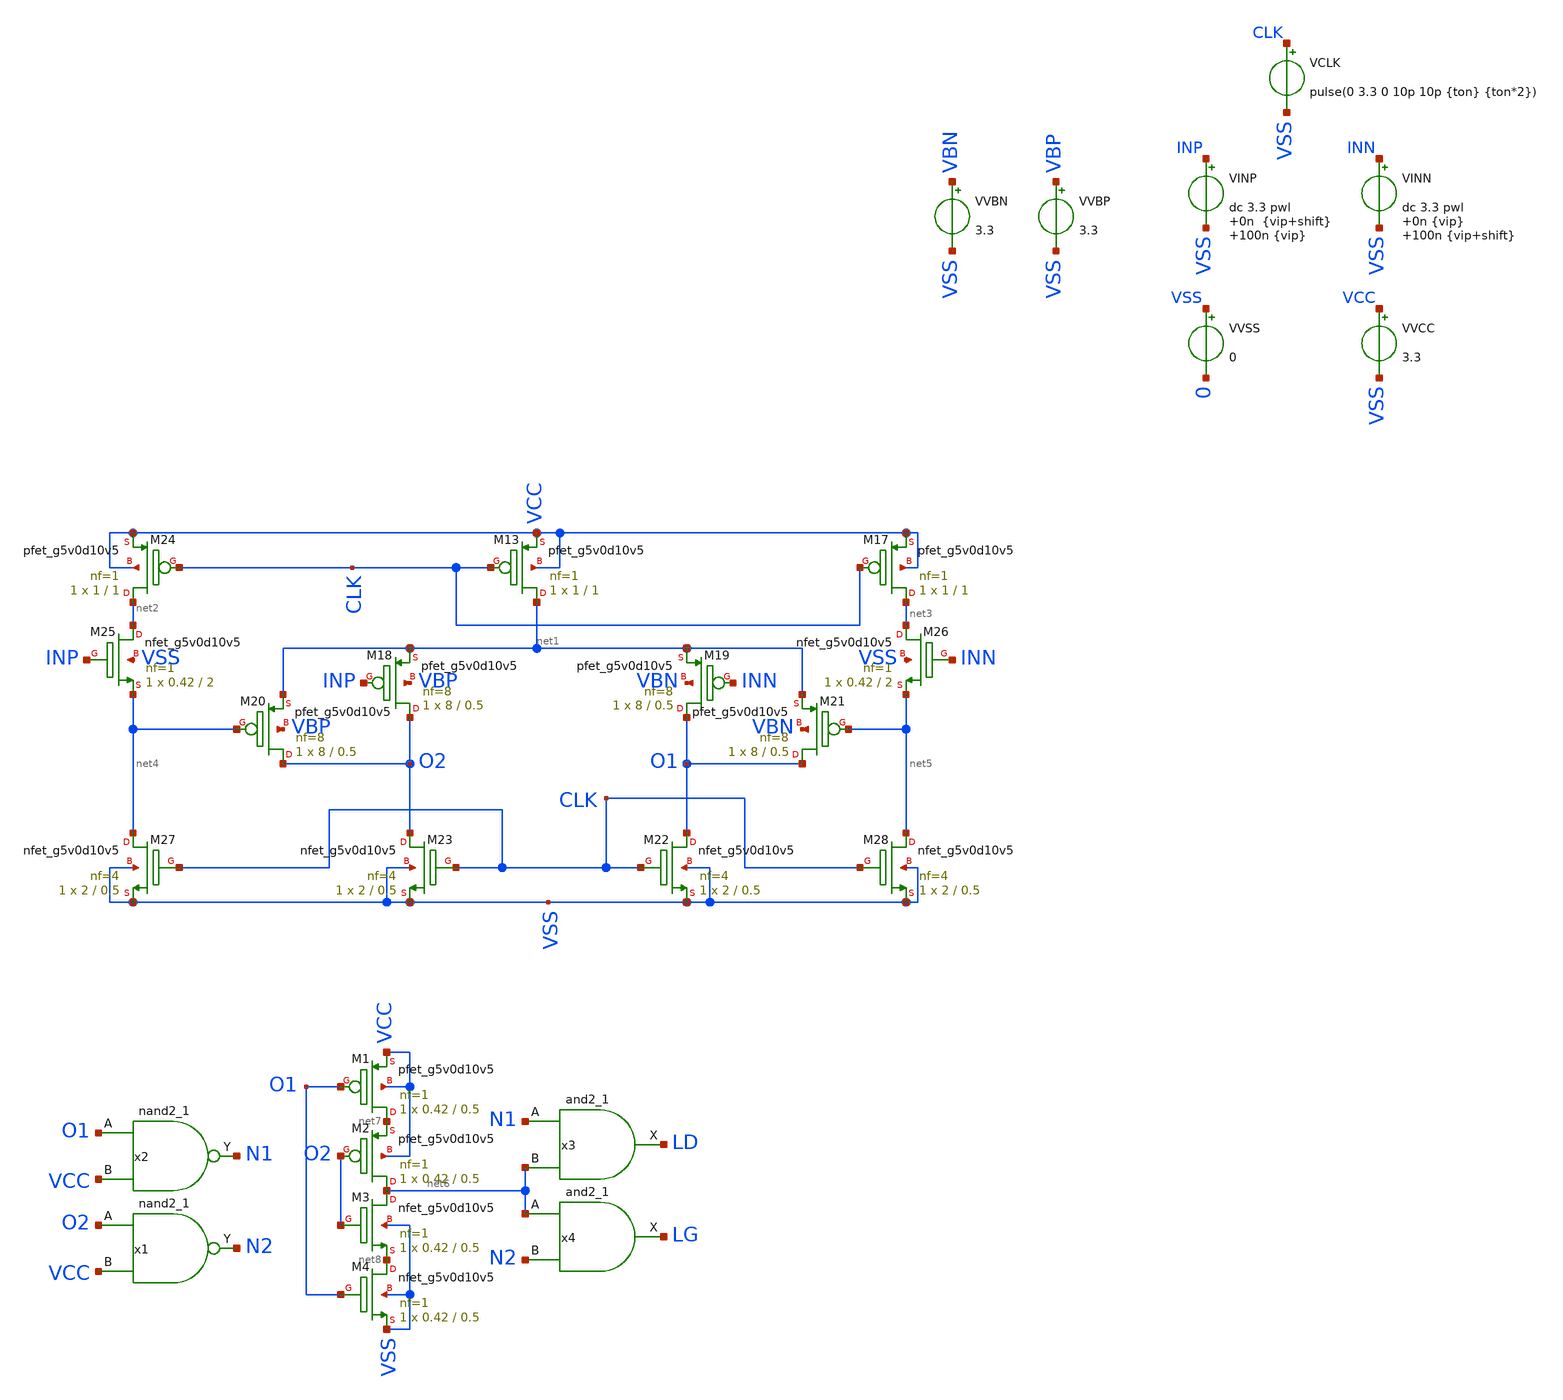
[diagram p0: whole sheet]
** sch_path: Comparator/schematic/new_comparator/c.sch
.lib $::SKYWATER_MODELS/sky130.lib.spice.tt.red tt_mm
.include $::SKYWATER_STDCELLS/sky130_fd_sc_hd.spice

**.subckt c
VINP INP VSS dc 3.3 pwl 0n {vip+shift} 100n {vip}
VINN INN VSS dc 3.3 pwl 0n {vip} 100n {vip+shift}
VVSS VSS 0 0
VVCC VCC VSS 3.3
VCLK CLK VSS pulse(0 3.3 0 10p 10p {ton} {ton*2})
XM13 net1 CLK VCC VCC sky130_fd_pr__pfet_g5v0d10v5 L=1 W=1 nf=1 ad='int((nf+1)/2) * W/nf * 0.29' as='int((nf+2)/2) * W/nf * 0.29'
+ pd='2*int((nf+1)/2) * (W/nf + 0.29)' ps='2*int((nf+2)/2) * (W/nf + 0.29)' nrd='0.29 / W' nrs='0.29 / W'
+ sa=0 sb=0 sd=0 mult=1 m=1
XM17 net3 CLK VCC VCC sky130_fd_pr__pfet_g5v0d10v5 L=1 W=1 nf=1 ad='int((nf+1)/2) * W/nf * 0.29' as='int((nf+2)/2) * W/nf * 0.29'
+ pd='2*int((nf+1)/2) * (W/nf + 0.29)' ps='2*int((nf+2)/2) * (W/nf + 0.29)' nrd='0.29 / W' nrs='0.29 / W'
+ sa=0 sb=0 sd=0 mult=1 m=1
XM18 O2 INP net1 VBP sky130_fd_pr__pfet_g5v0d10v5 L=0.5 W=8 nf=8 ad='int((nf+1)/2) * W/nf * 0.29' as='int((nf+2)/2) * W/nf * 0.29'
+ pd='2*int((nf+1)/2) * (W/nf + 0.29)' ps='2*int((nf+2)/2) * (W/nf + 0.29)' nrd='0.29 / W' nrs='0.29 / W'
+ sa=0 sb=0 sd=0 mult=1 m=1
XM19 O1 INN net1 VBN sky130_fd_pr__pfet_g5v0d10v5 L=0.5 W=8 nf=8 ad='int((nf+1)/2) * W/nf * 0.29' as='int((nf+2)/2) * W/nf * 0.29'
+ pd='2*int((nf+1)/2) * (W/nf + 0.29)' ps='2*int((nf+2)/2) * (W/nf + 0.29)' nrd='0.29 / W' nrs='0.29 / W'
+ sa=0 sb=0 sd=0 mult=1 m=1
XM20 O2 net4 net1 VBP sky130_fd_pr__pfet_g5v0d10v5 L=0.5 W=8 nf=8 ad='int((nf+1)/2) * W/nf * 0.29' as='int((nf+2)/2) * W/nf * 0.29'
+ pd='2*int((nf+1)/2) * (W/nf + 0.29)' ps='2*int((nf+2)/2) * (W/nf + 0.29)' nrd='0.29 / W' nrs='0.29 / W'
+ sa=0 sb=0 sd=0 mult=1 m=1
XM21 O1 net5 net1 VBN sky130_fd_pr__pfet_g5v0d10v5 L=0.5 W=8 nf=8 ad='int((nf+1)/2) * W/nf * 0.29' as='int((nf+2)/2) * W/nf * 0.29'
+ pd='2*int((nf+1)/2) * (W/nf + 0.29)' ps='2*int((nf+2)/2) * (W/nf + 0.29)' nrd='0.29 / W' nrs='0.29 / W'
+ sa=0 sb=0 sd=0 mult=1 m=1
XM22 O1 CLK VSS VSS sky130_fd_pr__nfet_g5v0d10v5 L=0.5 W=2 nf=4 ad='int((nf+1)/2) * W/nf * 0.29' as='int((nf+2)/2) * W/nf * 0.29'
+ pd='2*int((nf+1)/2) * (W/nf + 0.29)' ps='2*int((nf+2)/2) * (W/nf + 0.29)' nrd='0.29 / W' nrs='0.29 / W'
+ sa=0 sb=0 sd=0 mult=1 m=1
XM23 O2 CLK VSS VSS sky130_fd_pr__nfet_g5v0d10v5 L=0.5 W=2 nf=4 ad='int((nf+1)/2) * W/nf * 0.29' as='int((nf+2)/2) * W/nf * 0.29'
+ pd='2*int((nf+1)/2) * (W/nf + 0.29)' ps='2*int((nf+2)/2) * (W/nf + 0.29)' nrd='0.29 / W' nrs='0.29 / W'
+ sa=0 sb=0 sd=0 mult=1 m=1
XM24 net2 CLK VCC VCC sky130_fd_pr__pfet_g5v0d10v5 L=1 W=1 nf=1 ad='int((nf+1)/2) * W/nf * 0.29' as='int((nf+2)/2) * W/nf * 0.29'
+ pd='2*int((nf+1)/2) * (W/nf + 0.29)' ps='2*int((nf+2)/2) * (W/nf + 0.29)' nrd='0.29 / W' nrs='0.29 / W'
+ sa=0 sb=0 sd=0 mult=1 m=1
XM25 net2 INP net4 VSS sky130_fd_pr__nfet_g5v0d10v5 L=2 W=0.42 nf=1 ad='int((nf+1)/2) * W/nf * 0.29'
+ as='int((nf+2)/2) * W/nf * 0.29' pd='2*int((nf+1)/2) * (W/nf + 0.29)' ps='2*int((nf+2)/2) * (W/nf + 0.29)'
+ nrd='0.29 / W' nrs='0.29 / W' sa=0 sb=0 sd=0 mult=1 m=1
XM26 net3 INN net5 VSS sky130_fd_pr__nfet_g5v0d10v5 L=2 W=0.42 nf=1 ad='int((nf+1)/2) * W/nf * 0.29'
+ as='int((nf+2)/2) * W/nf * 0.29' pd='2*int((nf+1)/2) * (W/nf + 0.29)' ps='2*int((nf+2)/2) * (W/nf + 0.29)'
+ nrd='0.29 / W' nrs='0.29 / W' sa=0 sb=0 sd=0 mult=1 m=1
XM27 net4 CLK VSS VSS sky130_fd_pr__nfet_g5v0d10v5 L=0.5 W=2 nf=4 ad='int((nf+1)/2) * W/nf * 0.29' as='int((nf+2)/2) * W/nf * 0.29'
+ pd='2*int((nf+1)/2) * (W/nf + 0.29)' ps='2*int((nf+2)/2) * (W/nf + 0.29)' nrd='0.29 / W' nrs='0.29 / W'
+ sa=0 sb=0 sd=0 mult=1 m=1
XM28 net5 CLK VSS VSS sky130_fd_pr__nfet_g5v0d10v5 L=0.5 W=2 nf=4 ad='int((nf+1)/2) * W/nf * 0.29' as='int((nf+2)/2) * W/nf * 0.29'
+ pd='2*int((nf+1)/2) * (W/nf + 0.29)' ps='2*int((nf+2)/2) * (W/nf + 0.29)' nrd='0.29 / W' nrs='0.29 / W'
+ sa=0 sb=0 sd=0 mult=1 m=1
x2 O1 VCC VSS VSS VCC VCC N1 sky130_fd_sc_hd__nand2_1
x1 O2 VCC VSS VSS VCC VCC N2 sky130_fd_sc_hd__nand2_1
XM1 net7 O1 VCC VCC sky130_fd_pr__pfet_g5v0d10v5 L=0.5 W=0.42 nf=1 ad='int((nf+1)/2) * W/nf * 0.29' as='int((nf+2)/2) * W/nf * 0.29'
+ pd='2*int((nf+1)/2) * (W/nf + 0.29)' ps='2*int((nf+2)/2) * (W/nf + 0.29)' nrd='0.29 / W' nrs='0.29 / W'
+ sa=0 sb=0 sd=0 mult=1 m=1
XM2 net6 O2 net7 VCC sky130_fd_pr__pfet_g5v0d10v5 L=0.5 W=0.42 nf=1 ad='int((nf+1)/2) * W/nf * 0.29'
+ as='int((nf+2)/2) * W/nf * 0.29' pd='2*int((nf+1)/2) * (W/nf + 0.29)' ps='2*int((nf+2)/2) * (W/nf + 0.29)'
+ nrd='0.29 / W' nrs='0.29 / W' sa=0 sb=0 sd=0 mult=1 m=1
XM3 net6 O2 net8 VSS sky130_fd_pr__nfet_g5v0d10v5 L=0.5 W=0.42 nf=1 ad='int((nf+1)/2) * W/nf * 0.29'
+ as='int((nf+2)/2) * W/nf * 0.29' pd='2*int((nf+1)/2) * (W/nf + 0.29)' ps='2*int((nf+2)/2) * (W/nf + 0.29)'
+ nrd='0.29 / W' nrs='0.29 / W' sa=0 sb=0 sd=0 mult=1 m=1
XM4 net8 O1 VSS VSS sky130_fd_pr__nfet_g5v0d10v5 L=0.5 W=0.42 nf=1 ad='int((nf+1)/2) * W/nf * 0.29' as='int((nf+2)/2) * W/nf * 0.29'
+ pd='2*int((nf+1)/2) * (W/nf + 0.29)' ps='2*int((nf+2)/2) * (W/nf + 0.29)' nrd='0.29 / W' nrs='0.29 / W'
+ sa=0 sb=0 sd=0 mult=1 m=1
x3 N1 net6 VSS VSS VCC VCC LD sky130_fd_sc_hd__and2_1
x4 net6 N2 VSS VSS VCC VCC LG sky130_fd_sc_hd__and2_1
VVBP VBP VSS 3.3
VVBN VBN VSS 3.3
**** begin user architecture code


** this experimental option enables mos model bin
** selection based on W/NF instead of W
.option chgtol=4e-16 method=gear

.param ton = 20n
.param vip = 0.05
.param shift = 0.05

.control
  option seed = 1
  let mc_runs = 20
  let run = 1

  set o2_node = ' '   ; new variable containing string with space (will become a list of strings, see
+ below)
  set n1_node = ' '
  set n2_node = ' '
  set ldlg_node = ' '

  write comparator_mine.raw
  reset
  set appendwrite

  dowhile run < = mc_runs
    save all
    tran 100p 100n uic
    *write comparator_mine.raw
    let vdiff = v(o2)-v(o1)
    let ldlg = v(ld)-v(lg)
    set o2_node = ( $o2_node {$curplot}.vdiff )
    set n1_node = ( $n1_node {$curplot}.ld )
    set n2_node = ( $n2_node {$curplot}.lg )
    set ldlg = ( $ldlg {$curplot}.ldlg )
    let run = run + 1
    reset
  end

** loop end, start plotting **
set color0 = white
*set nolegend                  ; legend for 27 graphs is unreadable
*set units=degrees             ; phase in degrees
set xbrushwidth=2             ; increase linewidth of graphs
plot $o2_node
plot $ldlg

*quit
.endc



**** end user architecture code
**.ends
.end
